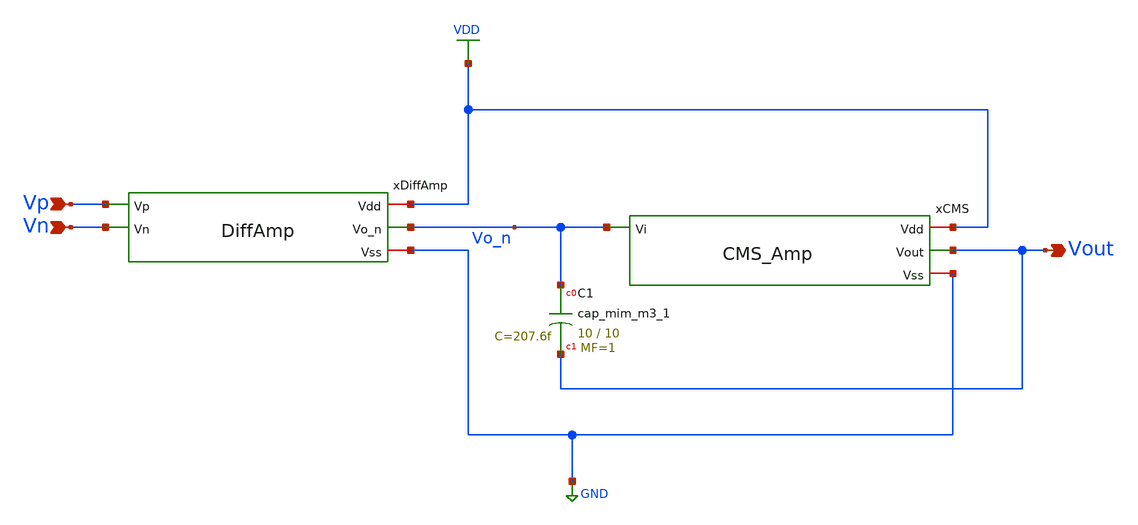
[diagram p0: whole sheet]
** sch_path: Circuits/DiffAmp/TwoStageDiffAmp.sch
**.subckt TwoStageDiffAmp Vout Vp Vn
*.opin Vout
*.ipin Vp
*.ipin Vn
xCMS VDD Vo_n Vout GND CMS_Amp
xDiffAmp VDD Vo_n Vp Vn GND DiffAmp
XC1 Vo_n Vout sky130_fd_pr__cap_mim_m3_1 W=10 L=10 MF=1 m=1
**.ends
.GLOBAL GND
.GLOBAL VDD
.end
